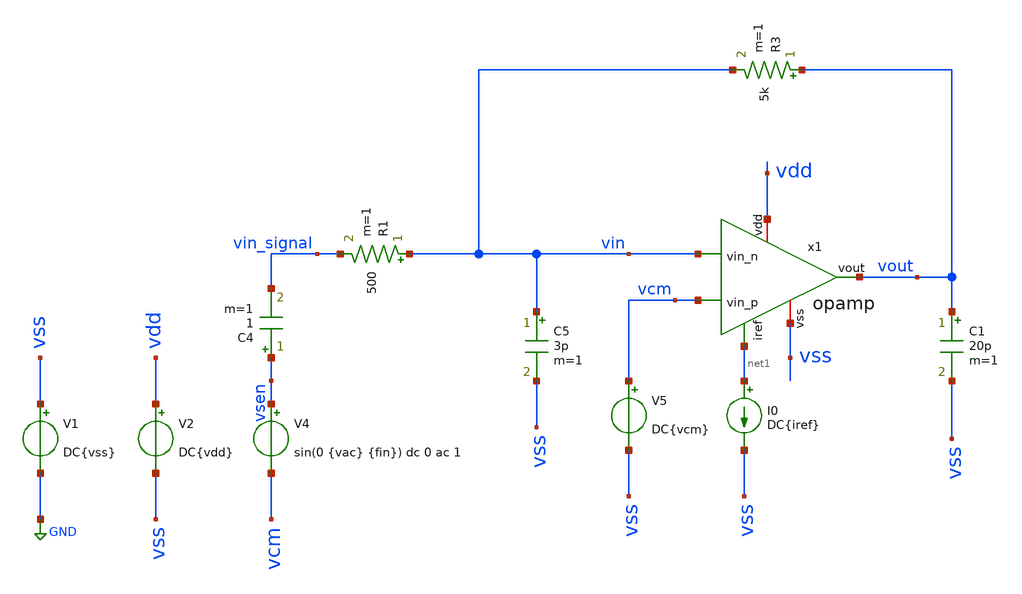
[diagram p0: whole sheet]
** sch_path: tb_opamp_closeloop.sch
**.subckt tb_opamp_closeloop
V1 vss GND DC{vss}
V2 vdd vss DC{vdd}
V4 vsen vcm sin(0 {vac} {fin}) dc 0 ac 1
C4 vsen vin_signal 1 m=1
I0 net1 vss DC{iref}
R1 vin vin_signal 500 m=1
R3 vout vin 5k m=1
C5 vin vss 3p m=1
C1 vout vss 20p m=1
V5 vcm vss DC{vcm}
x1 vdd net1 vin vcm vout vss opamp
**** begin user architecture code




* Circuit Parameters
.param w_mirror_1 = 65
.param l_mirror_1 = 0.6
.param m_mirror_1 = 10

.param w_par = 41
.param l_par = 0.49
.param m_par = 48

.param w_mirror_2 = 40
.param l_mirror_2 = 1.4
.param m_mirror_2 = 8
.param cc = 13.25p

.param branch_2 = 20

.param iref = 100u
.param vdd  = 1.8
.param vss  = 0.0
.param vcm  = 0.8
.param vac  = 60m
.param fin  = 9.765625e5
.options TEMP = 65

* FFT Parameters
.param Ts_FFT     = 1e-9
.csparam Ts_FFT   = {Ts_FFT}
.param fin_approx = 1e6
.param NFFT       = 4096
.csparam NFFT     = {NFFT}
.param vac_fin    = 'floor(fin_approx*Ts_FFT*NFFT)/Ts_FFT/NFFT'
.csparam Ti_FFT   = 3u
.csparam vac_fin  = {vac_fin}

* Include Models
.lib ~/skywater/skywater-pdk/libraries/sky130_fd_pr_ngspice/latest/models/corners/sky130.lib TT

* OP Parameters & Singals to save
.save all  @M.X1.XM1.msky130_fd_pr__pfet_01v8_lvt[id] @M.X1.XM1.msky130_fd_pr__pfet_01v8_lvt[vth] @M.X1.XM1.msky130_fd_pr__pfet_01v8_lvt[vgs] @M.X1.XM1.msky130_fd_pr__pfet_01v8_lvt[vds] @M.X1.XM1.msky130_fd_pr__pfet_01v8_lvt[vdsat] @M.X1.XM1.msky130_fd_pr__pfet_01v8_lvt[gm] @M.X1.XM1.msky130_fd_pr__pfet_01v8_lvt[gds]    @M.X1.XM2.msky130_fd_pr__pfet_01v8_lvt[id] @M.X1.XM2.msky130_fd_pr__pfet_01v8_lvt[vth] @M.X1.XM2.msky130_fd_pr__pfet_01v8_lvt[vgs] @M.X1.XM2.msky130_fd_pr__pfet_01v8_lvt[vds] @M.X1.XM2.msky130_fd_pr__pfet_01v8_lvt[vdsat] @M.X1.XM2.msky130_fd_pr__pfet_01v8_lvt[gm] @M.X1.XM2.msky130_fd_pr__pfet_01v8_lvt[gds] @M.X1.XM2.msky130_fd_pr__pfet_01v8_lvt[cgg]   @M.X1.XM3.msky130_fd_pr__nfet_01v8[id] @M.X1.XM3.msky130_fd_pr__nfet_01v8[vth] @M.X1.XM3.msky130_fd_pr__nfet_01v8[vgs] @M.X1.XM3.msky130_fd_pr__nfet_01v8[vds] @M.X1.XM3.msky130_fd_pr__nfet_01v8[vdsat] @M.X1.XM3.msky130_fd_pr__nfet_01v8[gm] @M.X1.XM3.msky130_fd_pr__nfet_01v8[gds]  @M.X1.XM4.msky130_fd_pr__nfet_01v8[id] @M.X1.XM4.msky130_fd_pr__nfet_01v8[vth] @M.X1.XM4.msky130_fd_pr__nfet_01v8[vgs] @M.X1.XM4.msky130_fd_pr__nfet_01v8[vds] @M.X1.XM4.msky130_fd_pr__nfet_01v8[vdsat] @M.X1.XM4.msky130_fd_pr__nfet_01v8[gm] @M.X1.XM4.msky130_fd_pr__nfet_01v8[gds]  @M.X1.XM5.msky130_fd_pr__pfet_01v8[id] @M.X1.XM5.msky130_fd_pr__pfet_01v8[vth] @M.X1.XM5.msky130_fd_pr__pfet_01v8[vgs] @M.X1.XM5.msky130_fd_pr__pfet_01v8[vds] @M.X1.XM5.msky130_fd_pr__pfet_01v8[vdsat] @M.X1.XM5.msky130_fd_pr__pfet_01v8[gm] @M.X1.XM5.msky130_fd_pr__pfet_01v8[gds]  @M.X1.XM6.msky130_fd_pr__nfet_01v8[id] @M.X1.XM6.msky130_fd_pr__nfet_01v8[vth] @M.X1.XM6.msky130_fd_pr__nfet_01v8[vgs] @M.X1.XM6.msky130_fd_pr__nfet_01v8[vds] @M.X1.XM6.msky130_fd_pr__nfet_01v8[vdsat] @M.X1.XM6.msky130_fd_pr__nfet_01v8[gm] @M.X1.XM6.msky130_fd_pr__nfet_01v8[gds] @M.X1.XM6.msky130_fd_pr__nfet_01v8[cgs]   @M.X1.XM7.msky130_fd_pr__pfet_01v8[id] @M.X1.XM7.msky130_fd_pr__pfet_01v8[vth] @M.X1.XM7.msky130_fd_pr__pfet_01v8[vgs] @M.X1.XM7.msky130_fd_pr__pfet_01v8[vds] @M.X1.XM7.msky130_fd_pr__pfet_01v8[vdsat] @M.X1.XM7.msky130_fd_pr__pfet_01v8[gm] @M.X1.XM7.msky130_fd_pr__pfet_01v8[gds]  @M.X1.XM8.msky130_fd_pr__pfet_01v8[id] @M.X1.XM8.msky130_fd_pr__pfet_01v8[vth] @M.X1.XM8.msky130_fd_pr__pfet_01v8[vgs] @M.X1.XM8.msky130_fd_pr__pfet_01v8[vds] @M.X1.XM8.msky130_fd_pr__pfet_01v8[vdsat] @M.X1.XM8.msky130_fd_pr__pfet_01v8[gm] @M.X1.XM8.msky130_fd_pr__pfet_01v8[gds]  @M.X1.XM9.msky130_fd_pr__nfet_01v8[id] @M.X1.XM9.msky130_fd_pr__nfet_01v8[vth] @M.X1.XM9.msky130_fd_pr__nfet_01v8[vgs] @M.X1.XM9.msky130_fd_pr__nfet_01v8[vds] @M.X1.XM9.msky130_fd_pr__nfet_01v8[vdsat] @M.X1.XM9.msky130_fd_pr__nfet_01v8[gm] @M.X1.XM9.msky130_fd_pr__nfet_01v8[gds]

*Simulation
.control
  set color0 = white

  ac dec 100 1k 10G
  setplot ac1
  meas ac GBW when vdb(vout)=0
  meas ac DCG find vdb(vout) at=1k
  plot vdb(vout) {vp(vout)*180/PI}

  reset
  tran 0.01u 11u
  setplot tran1
  plot v(vsen) v(vout)

  *reset
  *set sqrnoise
  *noise v(vout) V4 dec 100 1k 10G 1
  *setplot noise1
  *plot onoise_spectrum
  *plot sqrt(integ(onoise_spectrum))
  *let onoise_total_integrado = maximum(sqrt(integ(onoise_spectrum)))
  *print onoise_total_integrado

  reset
  noise v(vout) V4 dec 100 1k 10G 1
  setplot noise1
  plot onoise_spectrum
  setplot noise2
  print inoise_total
  print onoise_total
  print onoise_total.m.x1.xm1.msky130_fd_pr__pfet_01v8_lvt.1overf
  print onoise_total.m.x1.xm1.msky130_fd_pr__pfet_01v8_lvt.id
  print onoise_total.m.x1.xm2.msky130_fd_pr__pfet_01v8_lvt.1overf
  print onoise_total.m.x1.xm2.msky130_fd_pr__pfet_01v8_lvt.id
  print onoise_total.m.x1.xm3.msky130_fd_pr__nfet_01v8.1overf
  print onoise_total.m.x1.xm3.msky130_fd_pr__nfet_01v8.id
  print onoise_total.m.x1.xm4.msky130_fd_pr__nfet_01v8.1overf
  print onoise_total.m.x1.xm4.msky130_fd_pr__nfet_01v8.id
  print onoise_total.m.x1.xm5.msky130_fd_pr__pfet_01v8.1overf
  print onoise_total.m.x1.xm5.msky130_fd_pr__pfet_01v8.id
  print onoise_total.m.x1.xm6.msky130_fd_pr__nfet_01v8.1overf
  print onoise_total.m.x1.xm6.msky130_fd_pr__nfet_01v8.id
  print onoise_total.m.x1.xm7.msky130_fd_pr__pfet_01v8.1overf
  print onoise_total.m.x1.xm7.msky130_fd_pr__pfet_01v8.id
  vprint onoise_total.m.x1.xm8.msky130_fd_pr__pfet_01v8.1overf
  print onoise_total.m.x1.xm8.msky130_fd_pr__pfet_01v8.id
  set filetype=ascii
  write tpfinal_noise.raw

  reset
  tran 0.001u 11u
  fourier 9.765625e5 vout
  let THD_db = db(fourier11[1][3]/fourier11[1][1])
  print THD_db
  let lin-tstart = {Ti_FFT} $ skip the start - up phase
  let lin-tstep = {Ts_FFT}
  let lin-tstop = {Ti_FFT + (NFFT-1) * Ts_FFT} $ end earlier
  linearize vout
  set specwindow = none
  fft vout
  *plot mag(vout)
  plot db(mag(vout)) xlimit 0 20e6

  reset
  op
  setplot op1
  unset filetype
  write tb_opamp_closeloop.raw
.endc

.end


**** end user architecture code
**.ends

* expanding   symbol:  opamp.sym # of pins=6
** sym_path: opamp.sym
** sch_path: opamp.sch
.subckt opamp vdd iref vin_n vin_p vout vss
*.iopin vdd
*.iopin vss
*.ipin vin_n
*.ipin vin_p
*.ipin iref
*.opin vout
XM3 vbn vbn vss vss sky130_fd_pr__nfet_01v8 L={l_mirror_2} W={w_mirror_2} nf=1 ad='W * 0.29' as='W * 0.29'
+ pd='2 * (W + 0.29)' ps='2 * (W + 0.29)' nrd='0.29 / W' nrs='0.29 / W' sa=0 sb=0 sd=0 mult={m_mirror_2}
+ m={m_mirror_2}
XM4 voe1 vbn vss vss sky130_fd_pr__nfet_01v8 L={l_mirror_2} W={w_mirror_2} nf=1 ad='W * 0.29' as='W * 0.29'
+ pd='2 * (W + 0.29)' ps='2 * (W + 0.29)' nrd='0.29 / W' nrs='0.29 / W' sa=0 sb=0 sd=0 mult={m_mirror_2}
+ m={m_mirror_2}
XM5 vp iref vdd vdd sky130_fd_pr__pfet_01v8 L={l_mirror_1} W={w_mirror_1} nf=1 ad='W * 0.29' as='W * 0.29'
+ pd='2 * (W + 0.29)' ps='2 * (W + 0.29)' nrd='0.29 / W' nrs='0.29 / W' sa=0 sb=0 sd=0 mult=12*10 m=12*10
XM7 vout iref vdd vdd sky130_fd_pr__pfet_01v8 L={l_mirror_1} W={w_mirror_1} nf=1 ad='W * 0.29' as='W * 0.29'
+ pd='2 * (W + 0.29)' ps='2 * (W + 0.29)' nrd='0.29 / W' nrs='0.29 / W' sa=0 sb=0 sd=0 mult=18*10 m=18*10
XM8 iref iref vdd vdd sky130_fd_pr__pfet_01v8 L={l_mirror_1} W={w_mirror_1} nf=1 ad='W * 0.29' as='W * 0.29'
+ pd='2 * (W + 0.29)' ps='2 * (W + 0.29)' nrd='0.29 / W' nrs='0.29 / W' sa=0 sb=0 sd=0 mult={m_mirror_1}
+ m={m_mirror_1}
XM9 net1 vdd voe1 vss sky130_fd_pr__nfet_01v8 L=0.15 W=20 nf=1 ad='W * 0.29' as='W * 0.29' pd='2 * (W + 0.29)'
+ ps='2 * (W + 0.29)' nrd='0.29 / W' nrs='0.29 / W' sa=0 sb=0 sd=0 mult=1 m=1
XM6 vout voe1 vss vss sky130_fd_pr__nfet_01v8 L=0.3 W=39.46 nf=1 ad='W * 0.29' as='W * 0.29' pd='2 * (W + 0.29)'
+ ps='2 * (W + 0.29)' nrd='0.29 / W' nrs='0.29 / W' sa=0 sb=0 sd=0 mult=17 m=17
XM1 vbn vin_n vp vp sky130_fd_pr__pfet_01v8_lvt L={l_par} W={w_par} nf=1 ad='int((nf+1)/2) * W/nf * 0.29'
+ as='int((nf+2)/2) * W/nf * 0.29' pd='2*int((nf+1)/2) * (W/nf + 0.29)' ps='2*int((nf+2)/2) * (W/nf + 0.29)'
+ nrd='0.29 / W' nrs='0.29 / W' sa=0 sb=0 sd=0 mult={m_par} m={m_par}
XM2 voe1 vin_p vp vp sky130_fd_pr__pfet_01v8_lvt L={l_par} W={w_par} nf=1 ad='int((nf+1)/2) * W/nf * 0.29'
+ as='int((nf+2)/2) * W/nf * 0.29' pd='2*int((nf+1)/2) * (W/nf + 0.29)' ps='2*int((nf+2)/2) * (W/nf + 0.29)'
+ nrd='0.29 / W' nrs='0.29 / W' sa=0 sb=0 sd=0 mult={m_par} m={m_par}
C1 net1 vout {cc} m=1
.ends

.GLOBAL GND
.end
